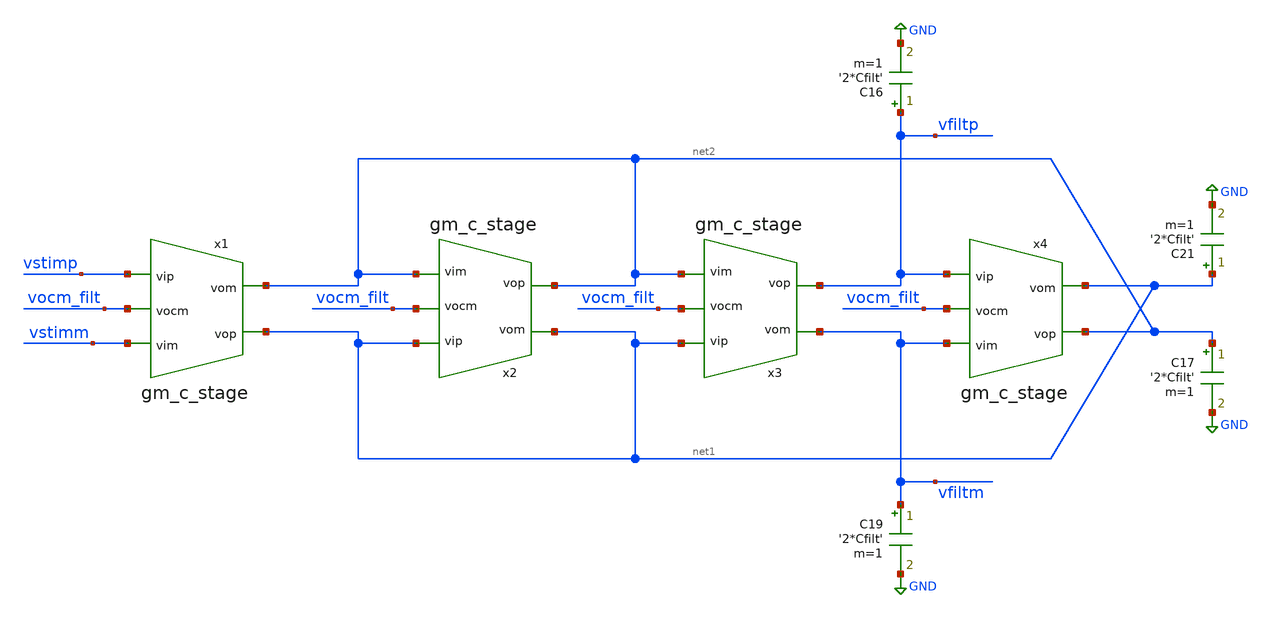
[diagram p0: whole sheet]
** sch_path: designs/active_lowpass_filter.sch
* Copyright 2020 Stefan Frederik Schippers
* Licensed under the Apache License, Version 2.0 (the "License");
* you may not use this file except in compliance with the License.
* You may obtain a copy of the License at
* https://www.apache.org/licenses/LICENSE-2.0
* Unless required by applicable law or agreed to in writing, software
* distributed under the License is distributed on an "AS IS" BASIS,
* WITHOUT WARRANTIES OR CONDITIONS OF ANY KIND, either express or implied.
* See the License for the specific language governing permissions and
* limitations under the License.
**.subckt active_lowpass_filter
C17 net2 GND '2*Cfilt' m=1
C21 net1 GND '2*Cfilt' m=1
C16 vfiltp GND '2*Cfilt' m=1
C19 vfiltm GND '2*Cfilt' m=1
x1 net2 net1 vstimp vstimm vocm_filt gm_c_stage Itail='Itail_filt' Wp=1 Wn_diff=8 Wpcm=1 Wncm=8 Wn_bias=1
+ Lp=1 Ln_diff=1 Lpcm=1 Lncm=1 Ln_bias=4
x2 net1 net2 net1 net2 vocm_filt gm_c_stage Itail='Itail_filt' Wp=1 Wn_diff=8 Wpcm=1 Wncm=8 Wn_bias=1
+ Lp=1 Ln_diff=1 Lpcm=1 Lncm=1 Ln_bias=4
x3 vfiltm vfiltp net1 net2 vocm_filt gm_c_stage Itail='Itail_filt' Wp=1 Wn_diff=8 Wpcm=1 Wncm=8 Wn_bias=1
+ Lp=1 Ln_diff=1 Lpcm=1 Lncm=1 Ln_bias=4
x4 net1 net2 vfiltp vfiltm vocm_filt gm_c_stage Itail='Itail_filt' Wp=1 Wn_diff=8 Wpcm=1 Wncm=8 Wn_bias=1
+ Lp=1 Ln_diff=1 Lpcm=1 Lncm=1 Ln_bias=4
**** begin user architecture code

.include $::SKYWATER_MODELS/cells/nfet_01v8/sky130_fd_pr__nfet_01v8__tt.corner.spice
.include $::SKYWATER_MODELS/cells/nfet_01v8_lvt/sky130_fd_pr__nfet_01v8_lvt__tt.corner.spice
.include $::SKYWATER_MODELS/cells/pfet_01v8/sky130_fd_pr__pfet_01v8__tt.corner.spice
.include $::SKYWATER_MODELS/cells/nfet_03v3_nvt/sky130_fd_pr__nfet_03v3_nvt__tt.corner.spice
.include $::SKYWATER_MODELS/cells/nfet_05v0_nvt/sky130_fd_pr__nfet_05v0_nvt__tt.corner.spice
.include $::SKYWATER_MODELS/cells/esd_nfet_01v8/sky130_fd_pr__esd_nfet_01v8__tt.corner.spice
.include $::SKYWATER_MODELS/cells/pfet_01v8_lvt/sky130_fd_pr__pfet_01v8_lvt__tt.corner.spice
.include $::SKYWATER_MODELS/cells/pfet_01v8_hvt/sky130_fd_pr__pfet_01v8_hvt__tt.corner.spice
.include $::SKYWATER_MODELS/cells/esd_pfet_g5v0d10v5/sky130_fd_pr__esd_pfet_g5v0d10v5__tt.corner.spice
.include $::SKYWATER_MODELS/cells/pfet_g5v0d10v5/sky130_fd_pr__pfet_g5v0d10v5__tt.corner.spice
.include $::SKYWATER_MODELS/cells/pfet_g5v0d16v0/sky130_fd_pr__pfet_g5v0d16v0__tt.corner.spice
.include $::SKYWATER_MODELS/cells/nfet_g5v0d10v5/sky130_fd_pr__nfet_g5v0d10v5__tt.corner.spice
.include $::SKYWATER_MODELS/cells/nfet_g5v0d16v0/sky130_fd_pr__nfet_g5v0d16v0__tt_discrete.corner.spice
.include $::SKYWATER_MODELS/cells/esd_nfet_g5v0d10v5/sky130_fd_pr__esd_nfet_g5v0d10v5__tt.corner.spice
.include $::SKYWATER_MODELS/models/corners/tt/nonfet.spice
* Mismatch parameters
.include $::SKYWATER_MODELS/cells/nfet_01v8/sky130_fd_pr__nfet_01v8__mismatch.corner.spice
.include $::SKYWATER_MODELS/cells/pfet_01v8/sky130_fd_pr__pfet_01v8__mismatch.corner.spice
.include $::SKYWATER_MODELS/cells/nfet_01v8_lvt/sky130_fd_pr__nfet_01v8_lvt__mismatch.corner.spice
.include $::SKYWATER_MODELS/cells/pfet_01v8_lvt/sky130_fd_pr__pfet_01v8_lvt__mismatch.corner.spice
.include $::SKYWATER_MODELS/cells/pfet_01v8_hvt/sky130_fd_pr__pfet_01v8_hvt__mismatch.corner.spice
.include $::SKYWATER_MODELS/cells/nfet_g5v0d10v5/sky130_fd_pr__nfet_g5v0d10v5__mismatch.corner.spice
.include $::SKYWATER_MODELS/cells/pfet_g5v0d10v5/sky130_fd_pr__pfet_g5v0d10v5__mismatch.corner.spice
.include $::SKYWATER_MODELS/cells/nfet_05v0_nvt/sky130_fd_pr__nfet_05v0_nvt__mismatch.corner.spice
.include $::SKYWATER_MODELS/cells/nfet_03v3_nvt/sky130_fd_pr__nfet_03v3_nvt__mismatch.corner.spice
* Resistor$::SKYWATER_MODELS/Capacitor
.include $::SKYWATER_MODELS/models/r+c/res_typical__cap_typical.spice
.include $::SKYWATER_MODELS/models/r+c/res_typical__cap_typical__lin.spice
* Special cells
.include $::SKYWATER_MODELS/models/corners/tt/specialized_cells.spice
* All models
.include $::SKYWATER_MODELS/models/all.spice
* Corner
.include $::SKYWATER_MODELS/models/corners/tt/rf.spice

**** end user architecture code
**.ends

* expanding   symbol:
*+  /home/users/nhpoole/ee272b/ee272b_mixed_signal_mmwave_accelerator/designs/gm_c_stage.sym # of pins=5
** sym_path: designs/gm_c_stage.sym
** sch_path: designs/gm_c_stage.sch
.subckt gm_c_stage vom vop vip vim vocm  Itail=0.01u Wp=0.5 Wn_diff=8 Wpcm=0.5 Wncm=8 Wn_bias=1 Lp=1
+ Ln_diff=1 Lpcm=1 Lncm=1 Ln_bias=4
*.ipin vip
*.ipin vim
*.ipin vocm
*.opin vop
*.opin vom
V6 vtail_diff net1 0
XM7 net1 vcmc_casc GND GND sky130_fd_pr__nfet_01v8 L='Ln_bias' W='Wn_bias' nf=1 ad='int((nf+1)/2) * W/nf * 0.29'
+ as='int((nf+2)/2) * W/nf * 0.29' pd='2*int((nf+1)/2) * (W/nf + 0.29)' ps='2*int((nf+2)/2) * (W/nf + 0.29)'
+ nrd='0.29 / W' nrs='0.29 / W' sa=0 sb=0 sd=0 mult=1 m=1
XM3 vcmn_casc_tail1 vnbiascm_casc GND GND sky130_fd_pr__nfet_01v8 L='Ln_bias' W='Wn_bias' nf=1 ad='int((nf+1)/2) * W/nf * 0.29'
+ as='int((nf+2)/2) * W/nf * 0.29' pd='2*int((nf+1)/2) * (W/nf + 0.29)' ps='2*int((nf+2)/2) * (W/nf + 0.29)'
+ nrd='0.29 / W' nrs='0.29 / W' sa=0 sb=0 sd=0 mult=1 m=1
XM10 vcmn_casc_tail2 vnbiascm_casc GND GND sky130_fd_pr__nfet_01v8 L='Ln_bias' W='Wn_bias' nf=1 ad='int((nf+1)/2) * W/nf * 0.29'
+ as='int((nf+2)/2) * W/nf * 0.29' pd='2*int((nf+1)/2) * (W/nf + 0.29)' ps='2*int((nf+2)/2) * (W/nf + 0.29)'
+ nrd='0.29 / W' nrs='0.29 / W' sa=0 sb=0 sd=0 mult=1 m=1
I4 VDD vnbiascm_casc 'Itail'
XM12 vnbiascm_casc vnbiascm_casc GND GND sky130_fd_pr__nfet_01v8 L='Ln_bias' W='Wn_bias' nf=1 ad='int((nf+1)/2) * W/nf * 0.29'
+ as='int((nf+2)/2) * W/nf * 0.29' pd='2*int((nf+1)/2) * (W/nf + 0.29)' ps='2*int((nf+2)/2) * (W/nf + 0.29)'
+ nrd='0.29 / W' nrs='0.29 / W' sa=0 sb=0 sd=0 mult=10 m=10
XM56 net2 vcmcn_casc VDD VDD sky130_fd_pr__pfet_01v8 L='Lpcm' W='Wpcm' nf=1 ad='int((nf+1)/2) * W/nf * 0.29'
+ as='int((nf+2)/2) * W/nf * 0.29' pd='2*int((nf+1)/2) * (W/nf + 0.29)' ps='2*int((nf+2)/2) * (W/nf + 0.29)'
+ nrd='0.29 / W' nrs='0.29 / W' sa=0 sb=0 sd=0 mult=1 m=1
V11 net2 vcmc_casc 0
XM13 vcmc_casc vcmc_casc GND GND sky130_fd_pr__nfet_01v8 L='Ln_bias' W='Wn_bias' nf=1 ad='int((nf+1)/2) * W/nf * 0.29'
+ as='int((nf+2)/2) * W/nf * 0.29' pd='2*int((nf+1)/2) * (W/nf + 0.29)' ps='2*int((nf+2)/2) * (W/nf + 0.29)'
+ nrd='0.29 / W' nrs='0.29 / W' sa=0 sb=0 sd=0 mult=1 m=1
XM14 net1 vnbiascm_casc GND GND sky130_fd_pr__nfet_01v8 L='Ln_bias' W='Wn_bias' nf=1 ad='int((nf+1)/2) * W/nf * 0.29'
+ as='int((nf+2)/2) * W/nf * 0.29' pd='2*int((nf+1)/2) * (W/nf + 0.29)' ps='2*int((nf+2)/2) * (W/nf + 0.29)'
+ nrd='0.29 / W' nrs='0.29 / W' sa=0 sb=0 sd=0 mult=1 m=1
XM4 vcmcn1_casc vcmcn1_casc VDD VDD sky130_fd_pr__pfet_01v8 L='Lpcm' W='Wpcm' nf=1 ad='int((nf+1)/2) * W/nf * 0.29'
+ as='int((nf+2)/2) * W/nf * 0.29' pd='2*int((nf+1)/2) * (W/nf + 0.29)' ps='2*int((nf+2)/2) * (W/nf + 0.29)'
+ nrd='0.29 / W' nrs='0.29 / W' sa=0 sb=0 sd=0 mult=1 m=1
XM5 vcmcn2_casc vcmcn2_casc VDD VDD sky130_fd_pr__pfet_01v8 L='Lpcm' W='Wpcm' nf=1 ad='int((nf+1)/2) * W/nf * 0.29'
+ as='int((nf+2)/2) * W/nf * 0.29' pd='2*int((nf+1)/2) * (W/nf + 0.29)' ps='2*int((nf+2)/2) * (W/nf + 0.29)'
+ nrd='0.29 / W' nrs='0.29 / W' sa=0 sb=0 sd=0 mult=1 m=1
XM6 vcmcn_casc vcmcn_casc VDD VDD sky130_fd_pr__pfet_01v8 L='Lpcm' W='Wpcm' nf=1 ad='int((nf+1)/2) * W/nf * 0.29'
+ as='int((nf+2)/2) * W/nf * 0.29' pd='2*int((nf+1)/2) * (W/nf + 0.29)' ps='2*int((nf+2)/2) * (W/nf + 0.29)'
+ nrd='0.29 / W' nrs='0.29 / W' sa=0 sb=0 sd=0 mult=1 m=1
XM15 net3 vnbiascm_casc GND GND sky130_fd_pr__nfet_01v8 L='Ln_bias' W='Wn_bias' nf=1 ad='int((nf+1)/2) * W/nf * 0.29'
+ as='int((nf+2)/2) * W/nf * 0.29' pd='2*int((nf+1)/2) * (W/nf + 0.29)' ps='2*int((nf+2)/2) * (W/nf + 0.29)'
+ nrd='0.29 / W' nrs='0.29 / W' sa=0 sb=0 sd=0 mult=1 m=1
XM8 net3 net3 VDD VDD sky130_fd_pr__pfet_01v8 L='Lp' W='Wp' nf=1 ad='int((nf+1)/2) * W/nf * 0.29' as='int((nf+2)/2) * W/nf * 0.29'
+ pd='2*int((nf+1)/2) * (W/nf + 0.29)' ps='2*int((nf+2)/2) * (W/nf + 0.29)' nrd='0.29 / W' nrs='0.29 / W'
+ sa=0 sb=0 sd=0 mult=1 m=1
XM9 vom net3 VDD VDD sky130_fd_pr__pfet_01v8 L='Lp' W='Wp' nf=1 ad='int((nf+1)/2) * W/nf * 0.29' as='int((nf+2)/2) * W/nf * 0.29'
+ pd='2*int((nf+1)/2) * (W/nf + 0.29)' ps='2*int((nf+2)/2) * (W/nf + 0.29)' nrd='0.29 / W' nrs='0.29 / W'
+ sa=0 sb=0 sd=0 mult=1 m=1
XM11 vop net3 VDD VDD sky130_fd_pr__pfet_01v8 L='Lp' W='Wp' nf=1 ad='int((nf+1)/2) * W/nf * 0.29' as='int((nf+2)/2) * W/nf * 0.29'
+ pd='2*int((nf+1)/2) * (W/nf + 0.29)' ps='2*int((nf+2)/2) * (W/nf + 0.29)' nrd='0.29 / W' nrs='0.29 / W'
+ sa=0 sb=0 sd=0 mult=1 m=1
XM16 vcmcn_casc vop vcmn_casc_tail1 GND sky130_fd_pr__nfet_01v8 L='Lncm' W='Wncm' nf=1 ad='int((nf+1)/2) * W/nf * 0.29'
+ as='int((nf+2)/2) * W/nf * 0.29' pd='2*int((nf+1)/2) * (W/nf + 0.29)' ps='2*int((nf+2)/2) * (W/nf + 0.29)'
+ nrd='0.29 / W' nrs='0.29 / W' sa=0 sb=0 sd=0 mult=1 m=1
XM17 vcmcn2_casc vocm vcmn_casc_tail2 GND sky130_fd_pr__nfet_01v8 L='Lncm' W='Wncm' nf=1 ad='int((nf+1)/2) * W/nf * 0.29'
+ as='int((nf+2)/2) * W/nf * 0.29' pd='2*int((nf+1)/2) * (W/nf + 0.29)' ps='2*int((nf+2)/2) * (W/nf + 0.29)'
+ nrd='0.29 / W' nrs='0.29 / W' sa=0 sb=0 sd=0 mult=1 m=1
XM18 vcmcn_casc vom vcmn_casc_tail2 GND sky130_fd_pr__nfet_01v8 L='Lncm' W='Wncm' nf=1 ad='int((nf+1)/2) * W/nf * 0.29'
+ as='int((nf+2)/2) * W/nf * 0.29' pd='2*int((nf+1)/2) * (W/nf + 0.29)' ps='2*int((nf+2)/2) * (W/nf + 0.29)'
+ nrd='0.29 / W' nrs='0.29 / W' sa=0 sb=0 sd=0 mult=1 m=1
XM19 vcmcn1_casc vocm vcmn_casc_tail1 GND sky130_fd_pr__nfet_01v8 L='Lncm' W='Wncm' nf=1 ad='int((nf+1)/2) * W/nf * 0.29'
+ as='int((nf+2)/2) * W/nf * 0.29' pd='2*int((nf+1)/2) * (W/nf + 0.29)' ps='2*int((nf+2)/2) * (W/nf + 0.29)'
+ nrd='0.29 / W' nrs='0.29 / W' sa=0 sb=0 sd=0 mult=1 m=1
XM1 vom vip vtail_diff GND sky130_fd_pr__nfet_01v8_lvt L='Ln_diff' W='Wn_diff' nf=1 ad='int((nf+1)/2) * W/nf * 0.29'
+ as='int((nf+2)/2) * W/nf * 0.29' pd='2*int((nf+1)/2) * (W/nf + 0.29)' ps='2*int((nf+2)/2) * (W/nf + 0.29)'
+ nrd='0.29 / W' nrs='0.29 / W' sa=0 sb=0 sd=0 mult=1 m=1
XM2 vop vim vtail_diff GND sky130_fd_pr__nfet_01v8_lvt L='Ln_diff' W='Wn_diff' nf=1 ad='int((nf+1)/2) * W/nf * 0.29'
+ as='int((nf+2)/2) * W/nf * 0.29' pd='2*int((nf+1)/2) * (W/nf + 0.29)' ps='2*int((nf+2)/2) * (W/nf + 0.29)'
+ nrd='0.29 / W' nrs='0.29 / W' sa=0 sb=0 sd=0 mult=1 m=1
.ends

.GLOBAL GND
.GLOBAL VDD
**** begin user architecture code

.include active_lowpass_filter_commands.spice

**** end user architecture code
.end
